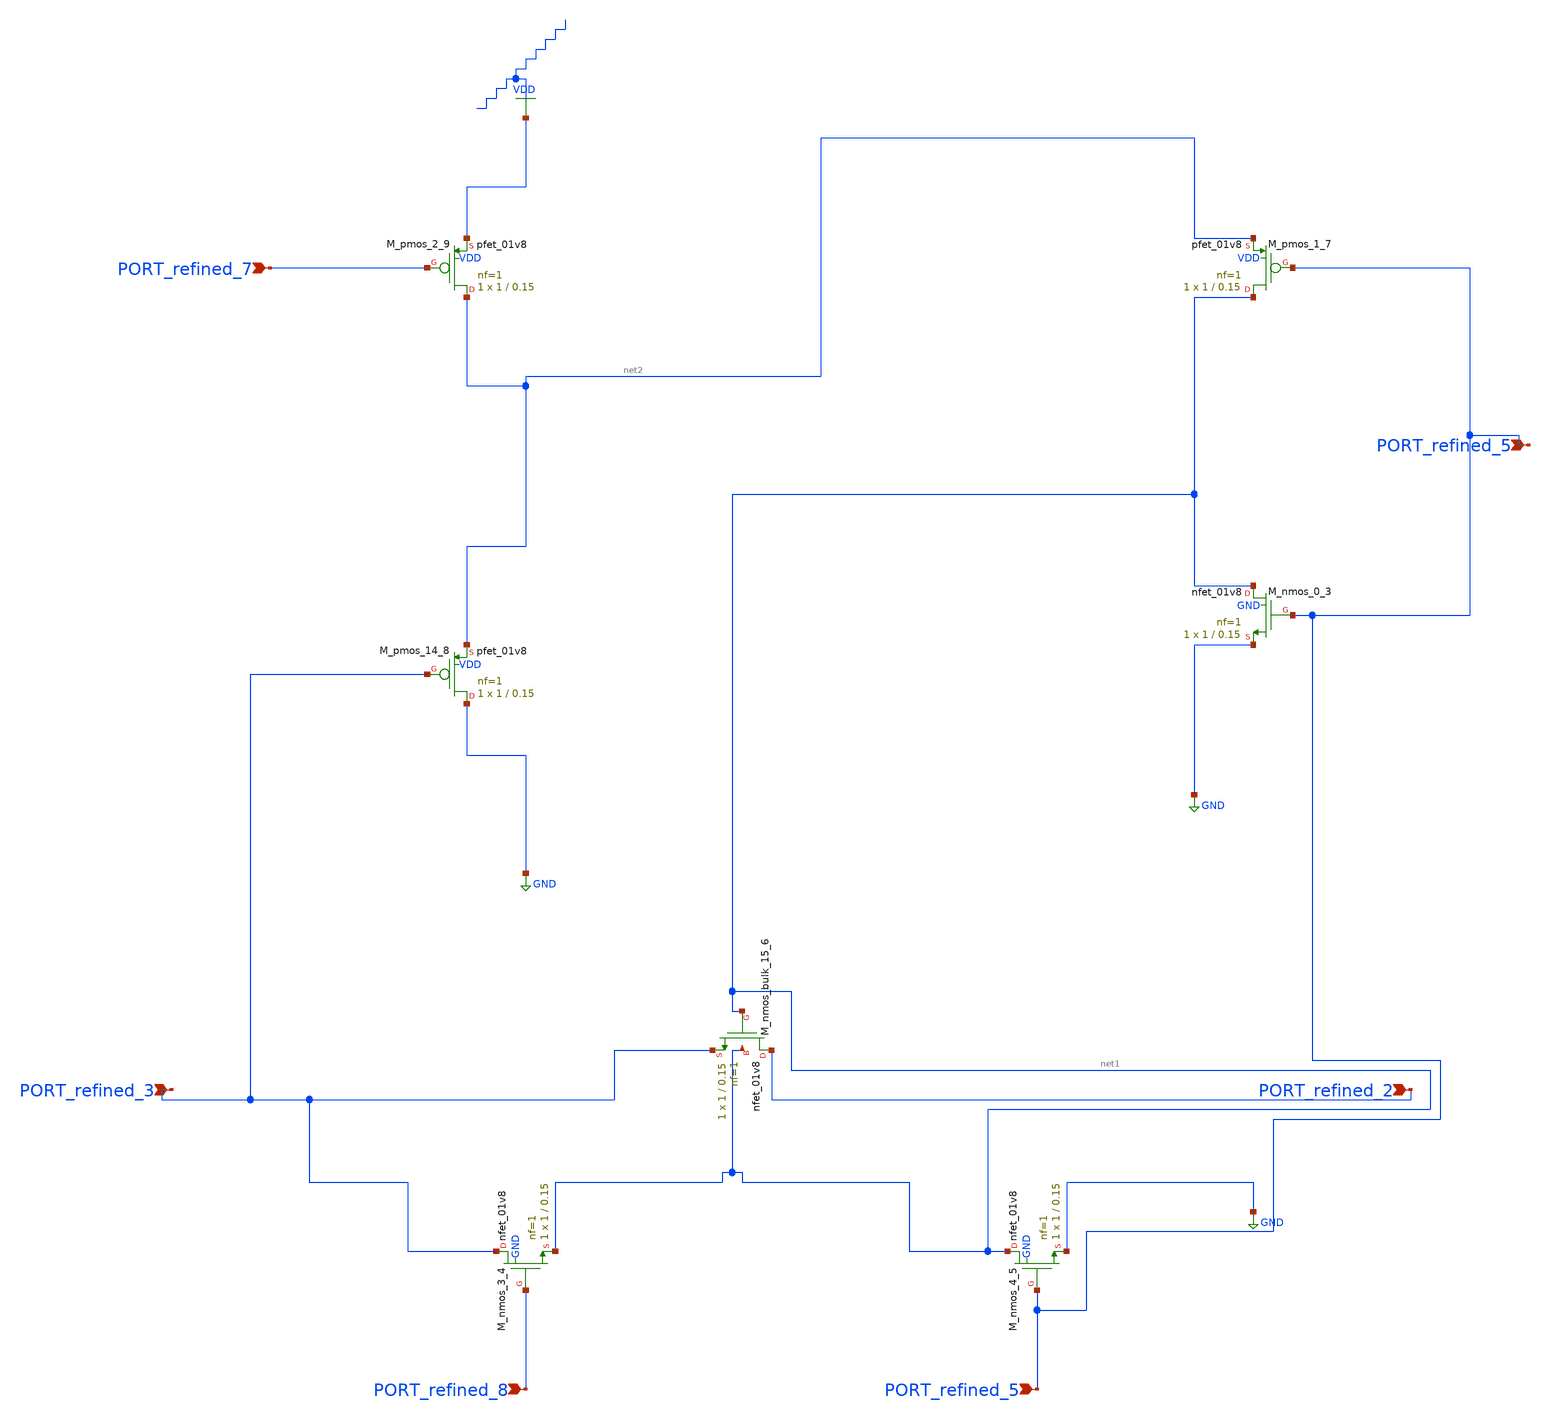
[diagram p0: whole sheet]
** sch_path: schematics/10_1007_s10470-010-9576-3_05_002.sch
**.subckt 10_1007_s10470-010-9576-3_05_002 PORT_refined_3 PORT_refined_7 PORT_refined_8
*+ PORT_refined_2 PORT_refined_5 PORT_refined_5
*.ipin PORT_refined_3
*.ipin PORT_refined_7
*.ipin PORT_refined_8
*.ipin PORT_refined_2
*.ipin PORT_refined_5
*.ipin PORT_refined_5
XM_nmos_0_3 net1 PORT_refined_5 GND GND sky130_fd_pr__nfet_01v8 L=0.15 W=1 nf=1 ad='int((1 + 1)/2) * 1 / 1 * 0.29'
+ as='int((1 + 2)/2) * 1 / 1 * 0.29' pd='2*int((1 + 1)/2) * (1 / 1 + 0.29)' ps='2*int((1 + 2)/2) * (1 / 1 + 0.29)'
+ nrd='0.29 / 1 ' nrs='0.29 / 1 ' sa=0 sb=0 sd=0 mult=1 m=1
XM_nmos_3_4 PORT_refined_3 PORT_refined_8 net1 GND sky130_fd_pr__nfet_01v8 L=0.15 W=1 nf=1 ad='int((1 + 1)/2) * 1 / 1 * 0.29'
+ as='int((1 + 2)/2) * 1 / 1 * 0.29' pd='2*int((1 + 1)/2) * (1 / 1 + 0.29)' ps='2*int((1 + 2)/2) * (1 / 1 + 0.29)'
+ nrd='0.29 / 1 ' nrs='0.29 / 1 ' sa=0 sb=0 sd=0 mult=1 m=1
XM_nmos_4_5 net1 PORT_refined_5 GND GND sky130_fd_pr__nfet_01v8 L=0.15 W=1 nf=1 ad='int((1 + 1)/2) * 1 / 1 * 0.29'
+ as='int((1 + 2)/2) * 1 / 1 * 0.29' pd='2*int((1 + 1)/2) * (1 / 1 + 0.29)' ps='2*int((1 + 2)/2) * (1 / 1 + 0.29)'
+ nrd='0.29 / 1 ' nrs='0.29 / 1 ' sa=0 sb=0 sd=0 mult=1 m=1
XM_nmos_bulk_15_6 PORT_refined_2 net1 PORT_refined_3 net1 sky130_fd_pr__nfet_01v8 L=0.15 W=1 nf=1 ad='int((1 + 1)/2) * 1 / 1 * 0.29'
+ as='int((1 + 2)/2) * 1 / 1 * 0.29' pd='2*int((1 + 1)/2) * (1 / 1 + 0.29)' ps='2*int((1 + 2)/2) * (1 / 1 + 0.29)'
+ nrd='0.29 / 1 ' nrs='0.29 / 1 ' sa=0 sb=0 sd=0 mult=1 m=1
XM_pmos_1_7 net1 PORT_refined_5 net2 VDD sky130_fd_pr__pfet_01v8 L=0.15 W=1 nf=1 ad='int((1 + 1)/2) * 1 / 1 * 0.29'
+ as='int((1 + 2)/2) * 1 / 1 * 0.29' pd='2*int((1 + 1)/2) * (1 / 1 + 0.29)' ps='2*int((1 + 2)/2) * (1 / 1 + 0.29)'
+ nrd='0.29 / 1 ' nrs='0.29 / 1 ' sa=0 sb=0 sd=0 mult=1 m=1
XM_pmos_14_8 GND PORT_refined_3 net2 VDD sky130_fd_pr__pfet_01v8 L=0.15 W=1 nf=1 ad='int((1 + 1)/2) * 1 / 1 * 0.29'
+ as='int((1 + 2)/2) * 1 / 1 * 0.29' pd='2*int((1 + 1)/2) * (1 / 1 + 0.29)' ps='2*int((1 + 2)/2) * (1 / 1 + 0.29)'
+ nrd='0.29 / 1 ' nrs='0.29 / 1 ' sa=0 sb=0 sd=0 mult=1 m=1
XM_pmos_2_9 net2 PORT_refined_7 VDD VDD sky130_fd_pr__pfet_01v8 L=0.15 W=1 nf=1 ad='int((1 + 1)/2) * 1 / 1 * 0.29'
+ as='int((1 + 2)/2) * 1 / 1 * 0.29' pd='2*int((1 + 1)/2) * (1 / 1 + 0.29)' ps='2*int((1 + 2)/2) * (1 / 1 + 0.29)'
+ nrd='0.29 / 1 ' nrs='0.29 / 1 ' sa=0 sb=0 sd=0 mult=1 m=1
**.ends
.GLOBAL GND
.GLOBAL VDD
.end
